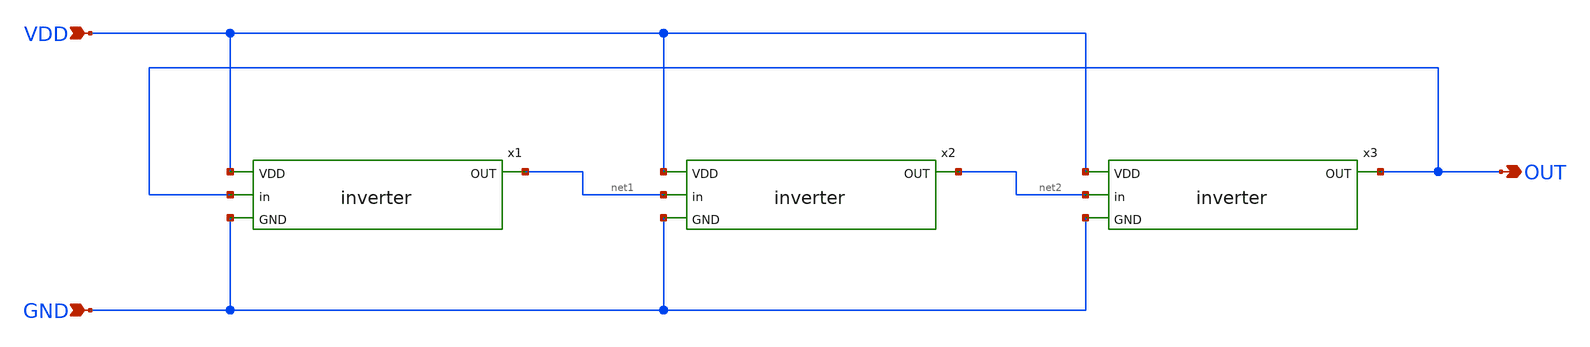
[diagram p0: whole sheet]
** sch_path: osic.sch
**.subckt osic GND VDD OUT
*.ipin GND
*.ipin VDD
*.opin OUT
x1 VDD OUT net1 GND inverter
x2 VDD net1 net2 GND inverter
x3 VDD net2 OUT GND inverter
**.ends

* expanding   symbol:  inverter.sym # of pins=4
** sym_path: inverter.sym
** sch_path: inverter.sch
.subckt inverter VDD in OUT GND
*.ipin in
*.ipin VDD
*.ipin GND
*.opin OUT
XM1 OUT in GND GND sky130_fd_pr__nfet_01v8 L=0.15 W=1 nf=1 ad='int((nf+1)/2) * W/nf * 0.29' as='int((nf+2)/2) * W/nf * 0.29'
+ pd='2*int((nf+1)/2) * (W/nf + 0.29)' ps='2*int((nf+2)/2) * (W/nf + 0.29)' nrd='0.29 / W' nrs='0.29 / W'
+ sa=0 sb=0 sd=0 mult=1 m=1
XM2 OUT in VDD VDD sky130_fd_pr__pfet_01v8 L=0.15 W=1 nf=1 ad='int((nf+1)/2) * W/nf * 0.29' as='int((nf+2)/2) * W/nf * 0.29'
+ pd='2*int((nf+1)/2) * (W/nf + 0.29)' ps='2*int((nf+2)/2) * (W/nf + 0.29)' nrd='0.29 / W' nrs='0.29 / W'
+ sa=0 sb=0 sd=0 mult=1 m=1
.ends

.end
